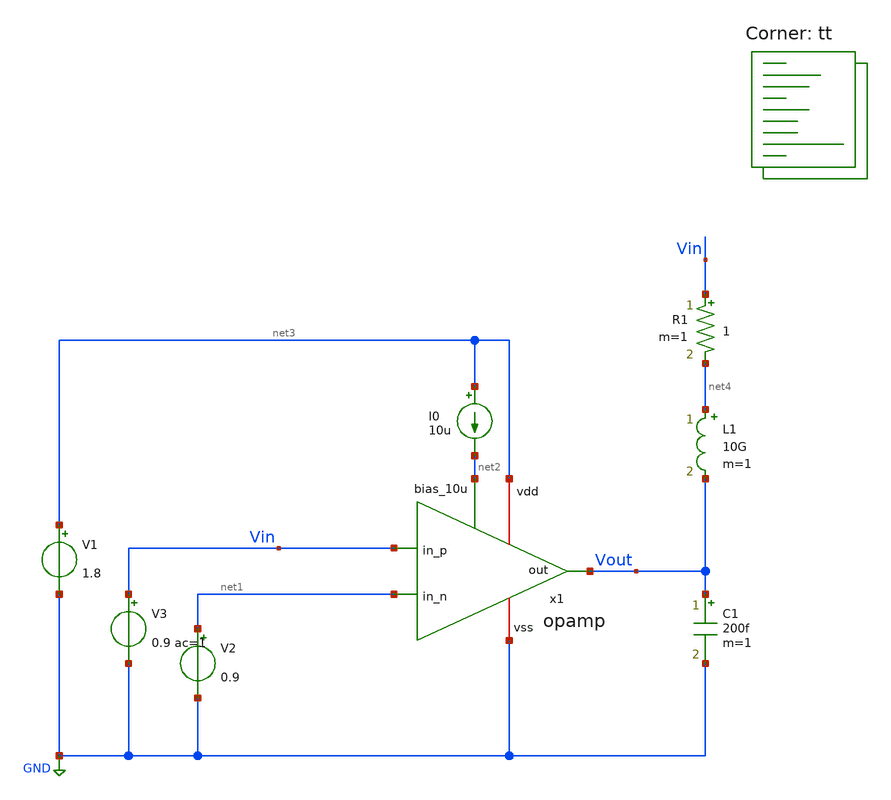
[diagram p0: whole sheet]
** sch_path: design/bgr_new/test_opamp_bode3.sch
**.subckt test_opamp_bode3
I0 net3 net2 10u
V1 net3 GND 1.8
V2 net1 GND 0.9
V3 Vin GND 0.9 ac=1
C1 Vout GND 200f m=1
x1 net3 net1 Vin Vout net2 GND opamp
L1 net4 Vout 10G m=1
R1 Vin net4 1 m=1
**** begin user architecture code


.param temp=27

.op
.ac dec 10 1 1G
*.tran 0.001 50n 20n

.control
ac dec 10 1 1G
let phase = 180/PI*vp(Vout)

plot vdb(Vout) phase
plot phase

.endc

.save all



.lib $::SKYWATER_MODELS/sky130.lib.spice tt
**** end user architecture code
**.ends

* expanding   symbol:  opamp/opamp.sym # of pins=6
** sym_path: design/opamp/opamp.sym
** sch_path: design/opamp/opamp.sch
.subckt opamp vdd in_n in_p out bias_10u vss
*.iopin vdd
*.iopin vss
*.ipin in_n
*.ipin in_p
*.opin out
*.ipin bias_10u
XM1 bias_10u bias_10u vss vss sky130_fd_pr__nfet_01v8_lvt L=2 W=1 nf=1 ad='int((nf+1)/2) * W/nf * 0.29'
+ as='int((nf+2)/2) * W/nf * 0.29' pd='2*int((nf+1)/2) * (W/nf + 0.29)' ps='2*int((nf+2)/2) * (W/nf + 0.29)'
+ nrd='0.29 / W' nrs='0.29 / W' sa=0 sb=0 sd=0 mult=1 m=1
XM_diff_n net3 in_n net1 vss sky130_fd_pr__nfet_01v8_lvt L=1 W=9 nf=1 ad='int((nf+1)/2) * W/nf * 0.29'
+ as='int((nf+2)/2) * W/nf * 0.29' pd='2*int((nf+1)/2) * (W/nf + 0.29)' ps='2*int((nf+2)/2) * (W/nf + 0.29)'
+ nrd='0.29 / W' nrs='0.29 / W' sa=0 sb=0 sd=0 mult=2 m=2
XM_diff_n1 net4 in_p net1 vss sky130_fd_pr__nfet_01v8_lvt L=1 W=9 nf=1 ad='int((nf+1)/2) * W/nf * 0.29'
+ as='int((nf+2)/2) * W/nf * 0.29' pd='2*int((nf+1)/2) * (W/nf + 0.29)' ps='2*int((nf+2)/2) * (W/nf + 0.29)'
+ nrd='0.29 / W' nrs='0.29 / W' sa=0 sb=0 sd=0 mult=2 m=2
XM_tail net1 net2 vss vss sky130_fd_pr__nfet_01v8_lvt L=4 W=5 nf=1 ad='int((nf+1)/2) * W/nf * 0.29' as='int((nf+2)/2) * W/nf * 0.29'
+ pd='2*int((nf+1)/2) * (W/nf + 0.29)' ps='2*int((nf+2)/2) * (W/nf + 0.29)' nrd='0.29 / W' nrs='0.29 / W'
+ sa=0 sb=0 sd=0 mult=8 m=8
XM_actload out net2 vss vss sky130_fd_pr__nfet_01v8_lvt L=2 W=4 nf=1 ad='int((nf+1)/2) * W/nf * 0.29'
+ as='int((nf+2)/2) * W/nf * 0.29' pd='2*int((nf+1)/2) * (W/nf + 0.29)' ps='2*int((nf+2)/2) * (W/nf + 0.29)'
+ nrd='0.29 / W' nrs='0.29 / W' sa=0 sb=0 sd=0 mult=6 m=6
XM_ppair_p net4 net3 vdd vdd sky130_fd_pr__pfet_01v8_lvt L=2 W=8 nf=1 ad='int((nf+1)/2) * W/nf * 0.29'
+ as='int((nf+2)/2) * W/nf * 0.29' pd='2*int((nf+1)/2) * (W/nf + 0.29)' ps='2*int((nf+2)/2) * (W/nf + 0.29)'
+ nrd='0.29 / W' nrs='0.29 / W' sa=0 sb=0 sd=0 mult=8 m=8
XM_ppair_p1 net3 net3 vdd vdd sky130_fd_pr__pfet_01v8_lvt L=2 W=8 nf=1 ad='int((nf+1)/2) * W/nf * 0.29'
+ as='int((nf+2)/2) * W/nf * 0.29' pd='2*int((nf+1)/2) * (W/nf + 0.29)' ps='2*int((nf+2)/2) * (W/nf + 0.29)'
+ nrd='0.29 / W' nrs='0.29 / W' sa=0 sb=0 sd=0 mult=8 m=8
XM_cs out net4 vdd vdd sky130_fd_pr__pfet_01v8_lvt L=0.5 W=12 nf=1 ad='int((nf+1)/2) * W/nf * 0.29' as='int((nf+2)/2) * W/nf * 0.29'
+ pd='2*int((nf+1)/2) * (W/nf + 0.29)' ps='2*int((nf+2)/2) * (W/nf + 0.29)' nrd='0.29 / W' nrs='0.29 / W'
+ sa=0 sb=0 sd=0 mult=12 m=12
V1 net2 vss 0.7
C1 net4 net5 150f m=1
R1 out net5 400 m=1
.ends

.GLOBAL GND
.end
